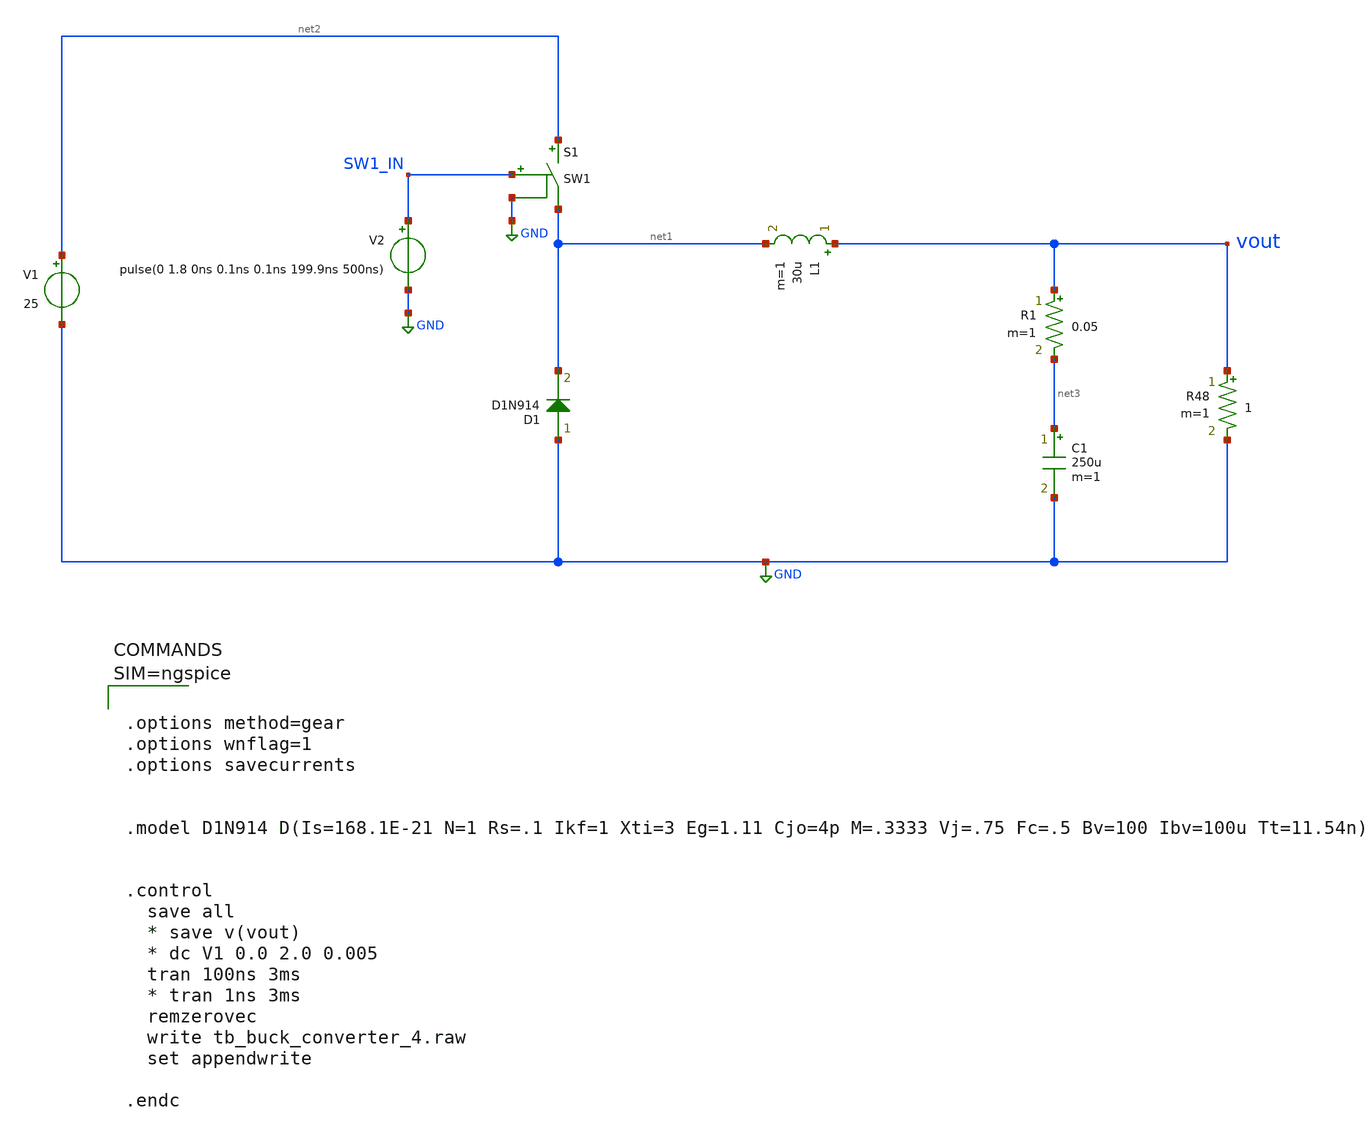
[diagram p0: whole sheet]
** sch_path: projects/ASU/EEE572/schematic/tb_buck_converter_4.sch
**.subckt tb_buck_converter_4
V1 net2 GND 25
R48 vout GND 1 m=1
L1 vout net1 30u m=1
C1 net3 GND 250u m=1
R1 vout net3 0.05 m=1
V2 SW1_IN GND pulse(0 1.8 0ns 0.1ns 0.1ns 199.9ns 500ns)
S1 net2 net1 SW1_IN GND SW1
D1 GND net1 D1N914 area=1
**** begin user architecture code



.options method=gear
.options wnflag=1
.options savecurrents


.model D1N914 D(Is=168.1E-21 N=1 Rs=.1 Ikf=1 Xti=3 Eg=1.11 Cjo=4p M=.3333 Vj=.75 Fc=.5 Bv=100
+ Ibv=100u Tt=11.54n)


.control
  save all
  * save v(vout)
  * dc V1 0.0 2.0 0.005
  tran 100ns 3ms
  * tran 1ns 3ms
  remzerovec
  write tb_buck_converter_4.raw
  set appendwrite

.endc





**** end user architecture code
**.ends
.GLOBAL GND
**** begin user architecture code
.MODEL SW1 SW( VT=0.9 VH=0.01 RON=0.01 ROFF=10G )
**** end user architecture code
.end
